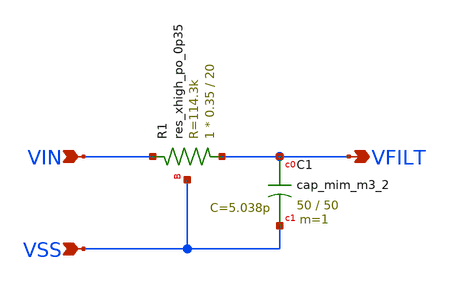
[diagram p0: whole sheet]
** sch_path: xschem/filter.sch
**.subckt filter VFILT VIN VSS
*.opin VFILT
*.ipin VIN
*.ipin VSS
XC1 VFILT VSS sky130_fd_pr__cap_mim_m3_2 W=50 L=50 MF=1 m=1
XR1 VFILT VIN VSS sky130_fd_pr__res_xhigh_po_0p35 L=20 mult=1 m=1
**.ends
.end
